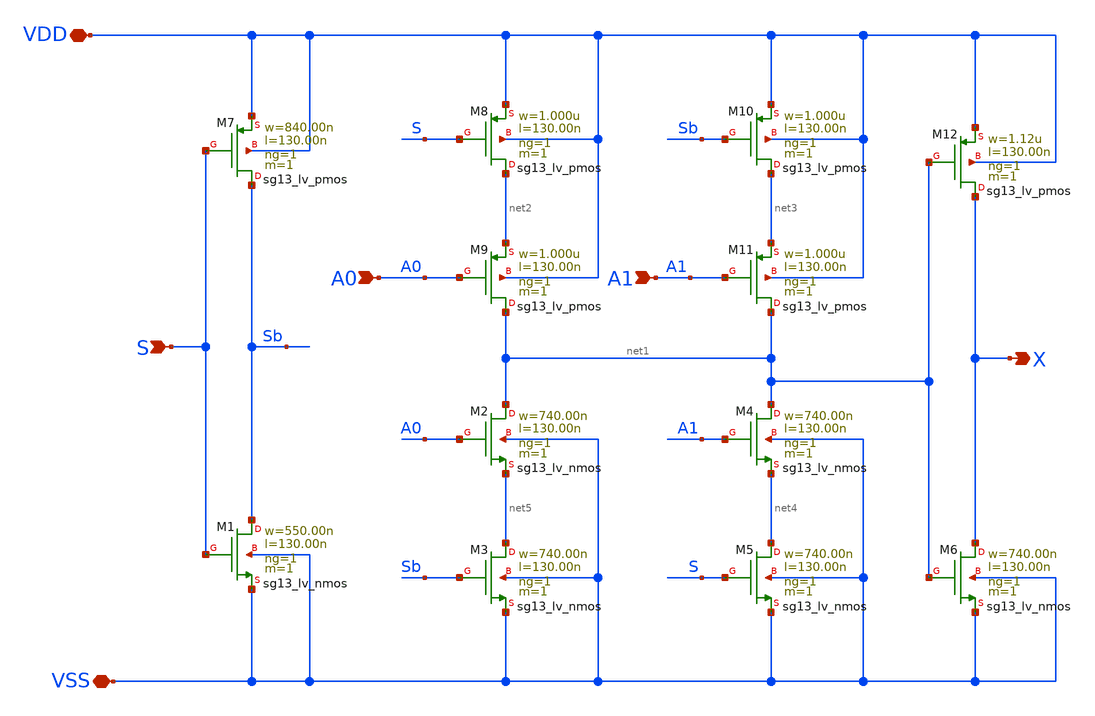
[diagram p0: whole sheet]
** sch_path: ihp-sg13g2/libs.tech/xschem/sg13g2_stdcells/sg13g2_mux2_1.sch
**.subckt sg13g2_mux2_1 S A0 A1 X VDD VSS
*.ipin S
*.ipin A0
*.ipin A1
*.opin X
*.iopin VDD
*.iopin VSS
XM1 Sb S VSS VSS sg13_lv_nmos w=550.00n l=130.00n ng=1 m=1 mm_ok=1
XM2 net1 A0 net5 VSS sg13_lv_nmos w=740.00n l=130.00n ng=1 m=1 mm_ok=1
XM3 net5 Sb VSS VSS sg13_lv_nmos w=740.00n l=130.00n ng=1 m=1 mm_ok=1
XM4 net1 A1 net4 VSS sg13_lv_nmos w=740.00n l=130.00n ng=1 m=1 mm_ok=1
XM5 net4 S VSS VSS sg13_lv_nmos w=740.00n l=130.00n ng=1 m=1 mm_ok=1
XM6 X net1 VSS VSS sg13_lv_nmos w=740.00n l=130.00n ng=1 m=1 mm_ok=1
XM7 Sb S VDD VDD sg13_lv_pmos w=840.00n l=130.00n ng=1 m=1 mm_ok=1
XM8 net2 S VDD VDD sg13_lv_pmos w=1.000u l=130.00n ng=1 m=1 mm_ok=1
XM9 net1 A0 net2 VDD sg13_lv_pmos w=1.000u l=130.00n ng=1 m=1 mm_ok=1
XM10 net3 Sb VDD VDD sg13_lv_pmos w=1.000u l=130.00n ng=1 m=1 mm_ok=1
XM11 net1 A1 net3 VDD sg13_lv_pmos w=1.000u l=130.00n ng=1 m=1 mm_ok=1
XM12 X net1 VDD VDD sg13_lv_pmos w=1.12u l=130.00n ng=1 m=1 mm_ok=1
**.ends
.end
